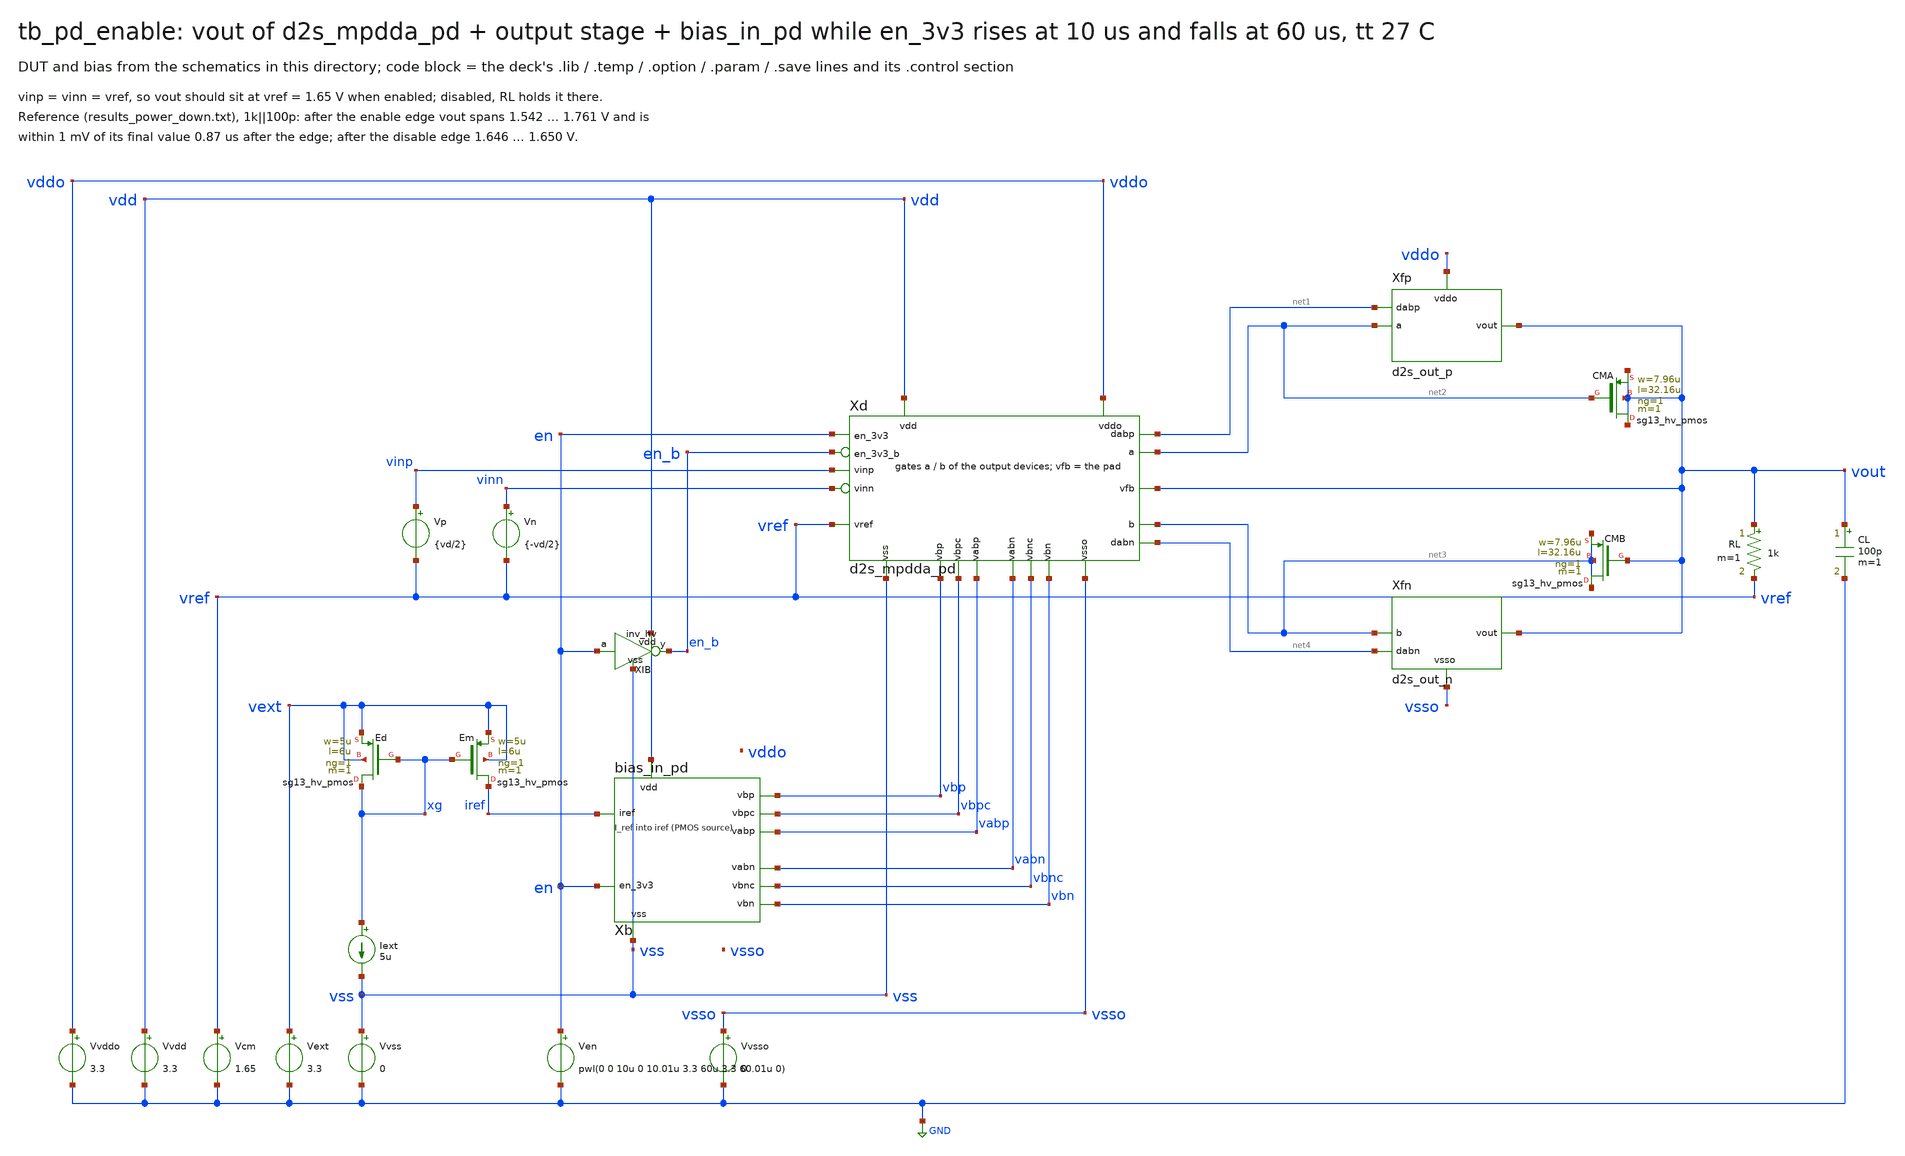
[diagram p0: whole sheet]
** sch_path: macros/sg13cmos5l_IOPadDiff2Single/testbenches/xschem/tb_pd_enable.sch
**.subckt tb_pd_enable
Vvdd vdd GND 3.3
Vvss vss GND 0
Vvddo vddo GND 3.3
Vvsso vsso GND 0
Ven en GND pwl(0 0 10u 0 10.01u 3.3 60u 3.3 60.01u 0)
Vext vext GND 3.3
Vcm vref GND 1.65
Xb vdd vss iref vbp vbn vbpc vbnc vabp vabn en bias_in_pd
Xd vdd vss vddo vsso vinp vinn vref vout net2 net3 net1 net4 vbp vbn vbpc vbnc vabp vabn en en_b
+ d2s_mpdda_pd
Vp vinp vref {vd/2}
Vn vinn vref {-vd/2}
XEd xg xg vext vext sg13_hv_pmos w=5u l=6u ng=1 m=1 mm_ok=1
XEm iref xg vext vext sg13_hv_pmos w=5u l=6u ng=1 m=1 mm_ok=1
Iext xg vss 5u
RL vout vref 1k m=1
CL vout GND 100p m=1
XIB vdd vss en en_b inv_hv
Xfp vddo net2 vout net1 d2s_out_p
Xfn vsso net3 vout net4 d2s_out_n
XCMA vout net2 vout vout sg13_hv_pmos w=7.96u l=32.16u ng=1 m=1 mm_ok=1
XCMB net3 vout net3 net3 sg13_hv_pmos w=7.96u l=32.16u ng=1 m=1 mm_ok=1
**** begin user architecture code

.lib cornerMOShv.lib mos_tt
.lib cornerRES.lib res_typ
.lib cornerCAP.lib cap_typ
.temp 27
.option method=gear
.param vd=0
.save v(vout) v(en) v(a) v(b) v(vbn) v(vbp)
.control
tran 2n 110u
meas tran vf find v(vout) at=59u
meas tran emin min v(vout) from=10u to=59u
meas tran emax max v(vout) from=10u to=59u
meas tran dmin min v(vout) from=60u to=62u
meas tran dmax max v(vout) from=60u to=62u
let dv = abs(v(vout) - vf)
meas tran tset when dv=1m cross=last from=10u to=59u
let t_1mV = tset - 10u
print vf emin emax t_1mV dmin dmax
if $?batchmode = 0
  plot v(vout) v(a) v(b) v(en)
end
.endc

**** end user architecture code
**.ends
.GLOBAL GND
.end
